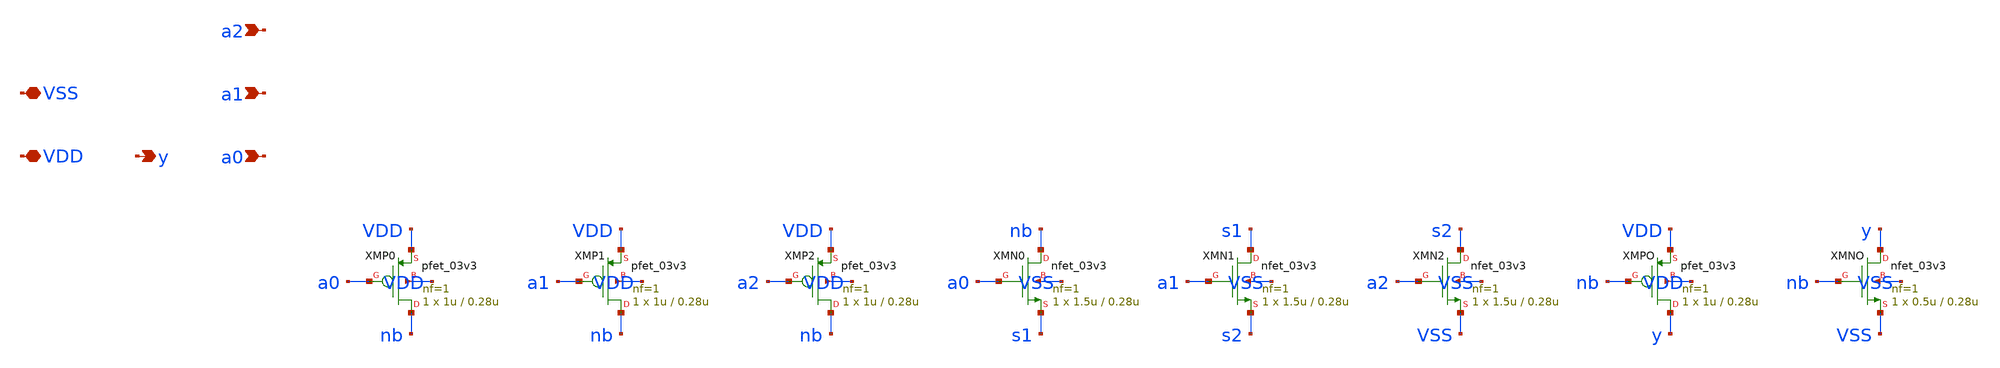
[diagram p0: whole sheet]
** sch_path: design/and3.sch
**.subckt and3 a0 a1 a2 y VDD VSS
*.ipin a0
*.ipin a1
*.ipin a2
*.opin y
*.iopin VDD
*.iopin VSS
XMP0 nb a0 VDD VDD pfet_03v3 L=0.28u W=1u nf=1 ad='int((nf+1)/2) * W/nf * 0.18u' as='int((nf+2)/2) * W/nf * 0.18u'
+ pd='2*int((nf+1)/2) * (W/nf + 0.18u)' ps='2*int((nf+2)/2) * (W/nf + 0.18u)' nrd='0.18u / W' nrs='0.18u / W'
+ sa=0 sb=0 sd=0 m=1
XMP1 nb a1 VDD VDD pfet_03v3 L=0.28u W=1u nf=1 ad='int((nf+1)/2) * W/nf * 0.18u' as='int((nf+2)/2) * W/nf * 0.18u'
+ pd='2*int((nf+1)/2) * (W/nf + 0.18u)' ps='2*int((nf+2)/2) * (W/nf + 0.18u)' nrd='0.18u / W' nrs='0.18u / W'
+ sa=0 sb=0 sd=0 m=1
XMP2 nb a2 VDD VDD pfet_03v3 L=0.28u W=1u nf=1 ad='int((nf+1)/2) * W/nf * 0.18u' as='int((nf+2)/2) * W/nf * 0.18u'
+ pd='2*int((nf+1)/2) * (W/nf + 0.18u)' ps='2*int((nf+2)/2) * (W/nf + 0.18u)' nrd='0.18u / W' nrs='0.18u / W'
+ sa=0 sb=0 sd=0 m=1
XMN0 nb a0 s1 VSS nfet_03v3 L=0.28u W=1.5u nf=1 ad='int((nf+1)/2) * W/nf * 0.18u' as='int((nf+2)/2) * W/nf * 0.18u'
+ pd='2*int((nf+1)/2) * (W/nf + 0.18u)' ps='2*int((nf+2)/2) * (W/nf + 0.18u)' nrd='0.18u / W' nrs='0.18u / W'
+ sa=0 sb=0 sd=0 m=1
XMN1 s1 a1 s2 VSS nfet_03v3 L=0.28u W=1.5u nf=1 ad='int((nf+1)/2) * W/nf * 0.18u' as='int((nf+2)/2) * W/nf * 0.18u'
+ pd='2*int((nf+1)/2) * (W/nf + 0.18u)' ps='2*int((nf+2)/2) * (W/nf + 0.18u)' nrd='0.18u / W' nrs='0.18u / W'
+ sa=0 sb=0 sd=0 m=1
XMN2 s2 a2 VSS VSS nfet_03v3 L=0.28u W=1.5u nf=1 ad='int((nf+1)/2) * W/nf * 0.18u' as='int((nf+2)/2) * W/nf * 0.18u'
+ pd='2*int((nf+1)/2) * (W/nf + 0.18u)' ps='2*int((nf+2)/2) * (W/nf + 0.18u)' nrd='0.18u / W' nrs='0.18u / W'
+ sa=0 sb=0 sd=0 m=1
XMPO y nb VDD VDD pfet_03v3 L=0.28u W=1u nf=1 ad='int((nf+1)/2) * W/nf * 0.18u' as='int((nf+2)/2) * W/nf * 0.18u'
+ pd='2*int((nf+1)/2) * (W/nf + 0.18u)' ps='2*int((nf+2)/2) * (W/nf + 0.18u)' nrd='0.18u / W' nrs='0.18u / W'
+ sa=0 sb=0 sd=0 m=1
XMNO y nb VSS VSS nfet_03v3 L=0.28u W=0.5u nf=1 ad='int((nf+1)/2) * W/nf * 0.18u' as='int((nf+2)/2) * W/nf * 0.18u'
+ pd='2*int((nf+1)/2) * (W/nf + 0.18u)' ps='2*int((nf+2)/2) * (W/nf + 0.18u)' nrd='0.18u / W' nrs='0.18u / W'
+ sa=0 sb=0 sd=0 m=1
**.ends
.end
